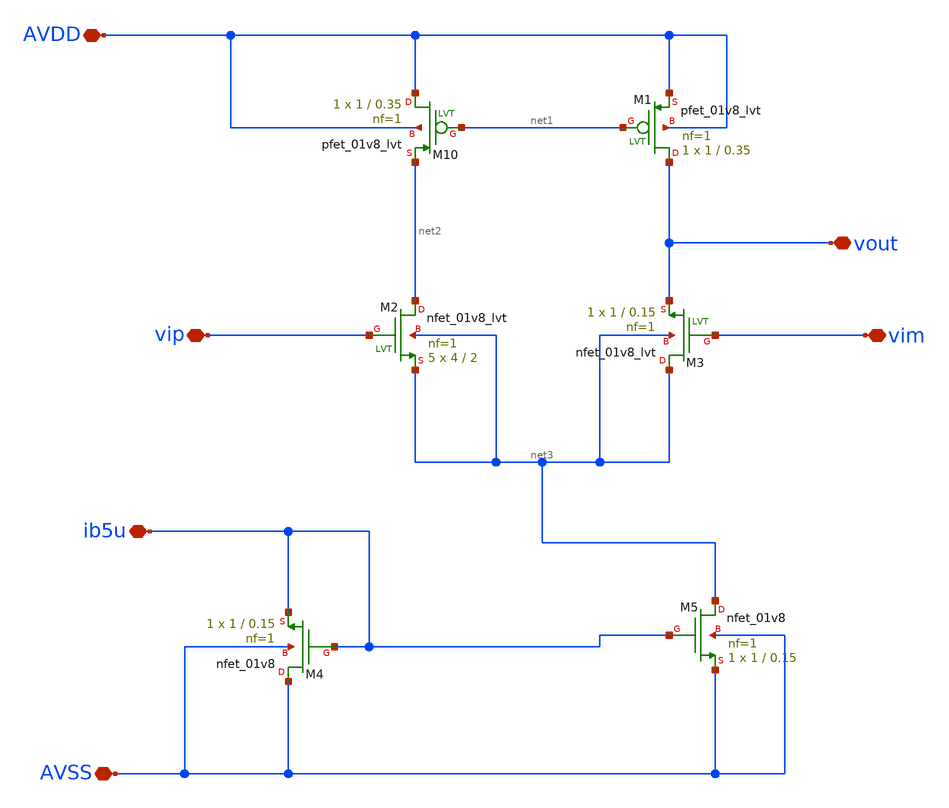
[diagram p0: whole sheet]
** sch_path: xschem/untitled-8.sch
**.subckt untitled-8 vip AVSS AVDD ib5u vim vout
*.iopin vip
*.iopin AVSS
*.iopin AVDD
*.iopin ib5u
*.iopin vim
*.iopin vout
XM10 AVDD net1 net2 AVDD sky130_fd_pr__pfet_01v8_lvt L=0.35 W=1 nf=1 ad='int((1 + 1)/2) * 1 / 1 * 0.29'
+ as='int((1 + 2)/2) * 1 / 1 * 0.29' pd='2*int((1 + 1)/2) * (1 / 1 + 0.29)' ps='2*int((1 + 2)/2) * (1 / 1 + 0.29)'
+ nrd='0.29 / 1 ' nrs='0.29 / 1 ' sa=0 sb=0 sd=0 mult=1 m=1
XM1 vout net1 AVDD AVDD sky130_fd_pr__pfet_01v8_lvt L=0.35 W=1 nf=1 ad='int((1 + 1)/2) * 1 / 1 * 0.29'
+ as='int((1 + 2)/2) * 1 / 1 * 0.29' pd='2*int((1 + 1)/2) * (1 / 1 + 0.29)' ps='2*int((1 + 2)/2) * (1 / 1 + 0.29)'
+ nrd='0.29 / 1 ' nrs='0.29 / 1 ' sa=0 sb=0 sd=0 mult=1 m=1
XM2 net2 vip net3 net3 sky130_fd_pr__nfet_01v8_lvt L=2 W=4 nf=1 ad='int((1 + 1)/2) * 4 / 1 * 0.29' as='int((1 + 2)/2) * 4 / 1 * 0.29'
+ pd='2*int((1 + 1)/2) * (4 / 1 + 0.29)' ps='2*int((1 + 2)/2) * (4 / 1 + 0.29)' nrd='0.29 / 4 ' nrs='0.29 / 4 '
+ sa=0 sb=0 sd=0 mult=5 m=5
XM3 net3 vim vout net3 sky130_fd_pr__nfet_01v8_lvt L=0.15 W=1 nf=1 ad='int((1 + 1)/2) * 1 / 1 * 0.29'
+ as='int((1 + 2)/2) * 1 / 1 * 0.29' pd='2*int((1 + 1)/2) * (1 / 1 + 0.29)' ps='2*int((1 + 2)/2) * (1 / 1 + 0.29)'
+ nrd='0.29 / 1 ' nrs='0.29 / 1 ' sa=0 sb=0 sd=0 mult=1 m=1
XM4 AVSS ib5u ib5u AVSS sky130_fd_pr__nfet_01v8 L=0.15 W=1 nf=1 ad='int((1 + 1)/2) * 1 / 1 * 0.29' as='int((1 + 2)/2) * 1 / 1 * 0.29'
+ pd='2*int((1 + 1)/2) * (1 / 1 + 0.29)' ps='2*int((1 + 2)/2) * (1 / 1 + 0.29)' nrd='0.29 / 1 ' nrs='0.29 / 1 '
+ sa=0 sb=0 sd=0 mult=1 m=1
XM5 net3 ib5u AVSS AVSS sky130_fd_pr__nfet_01v8 L=0.15 W=1 nf=1 ad='int((1 + 1)/2) * 1 / 1 * 0.29' as='int((1 + 2)/2) * 1 / 1 * 0.29'
+ pd='2*int((1 + 1)/2) * (1 / 1 + 0.29)' ps='2*int((1 + 2)/2) * (1 / 1 + 0.29)' nrd='0.29 / 1 ' nrs='0.29 / 1 '
+ sa=0 sb=0 sd=0 mult=1 m=1
**.ends
.end
